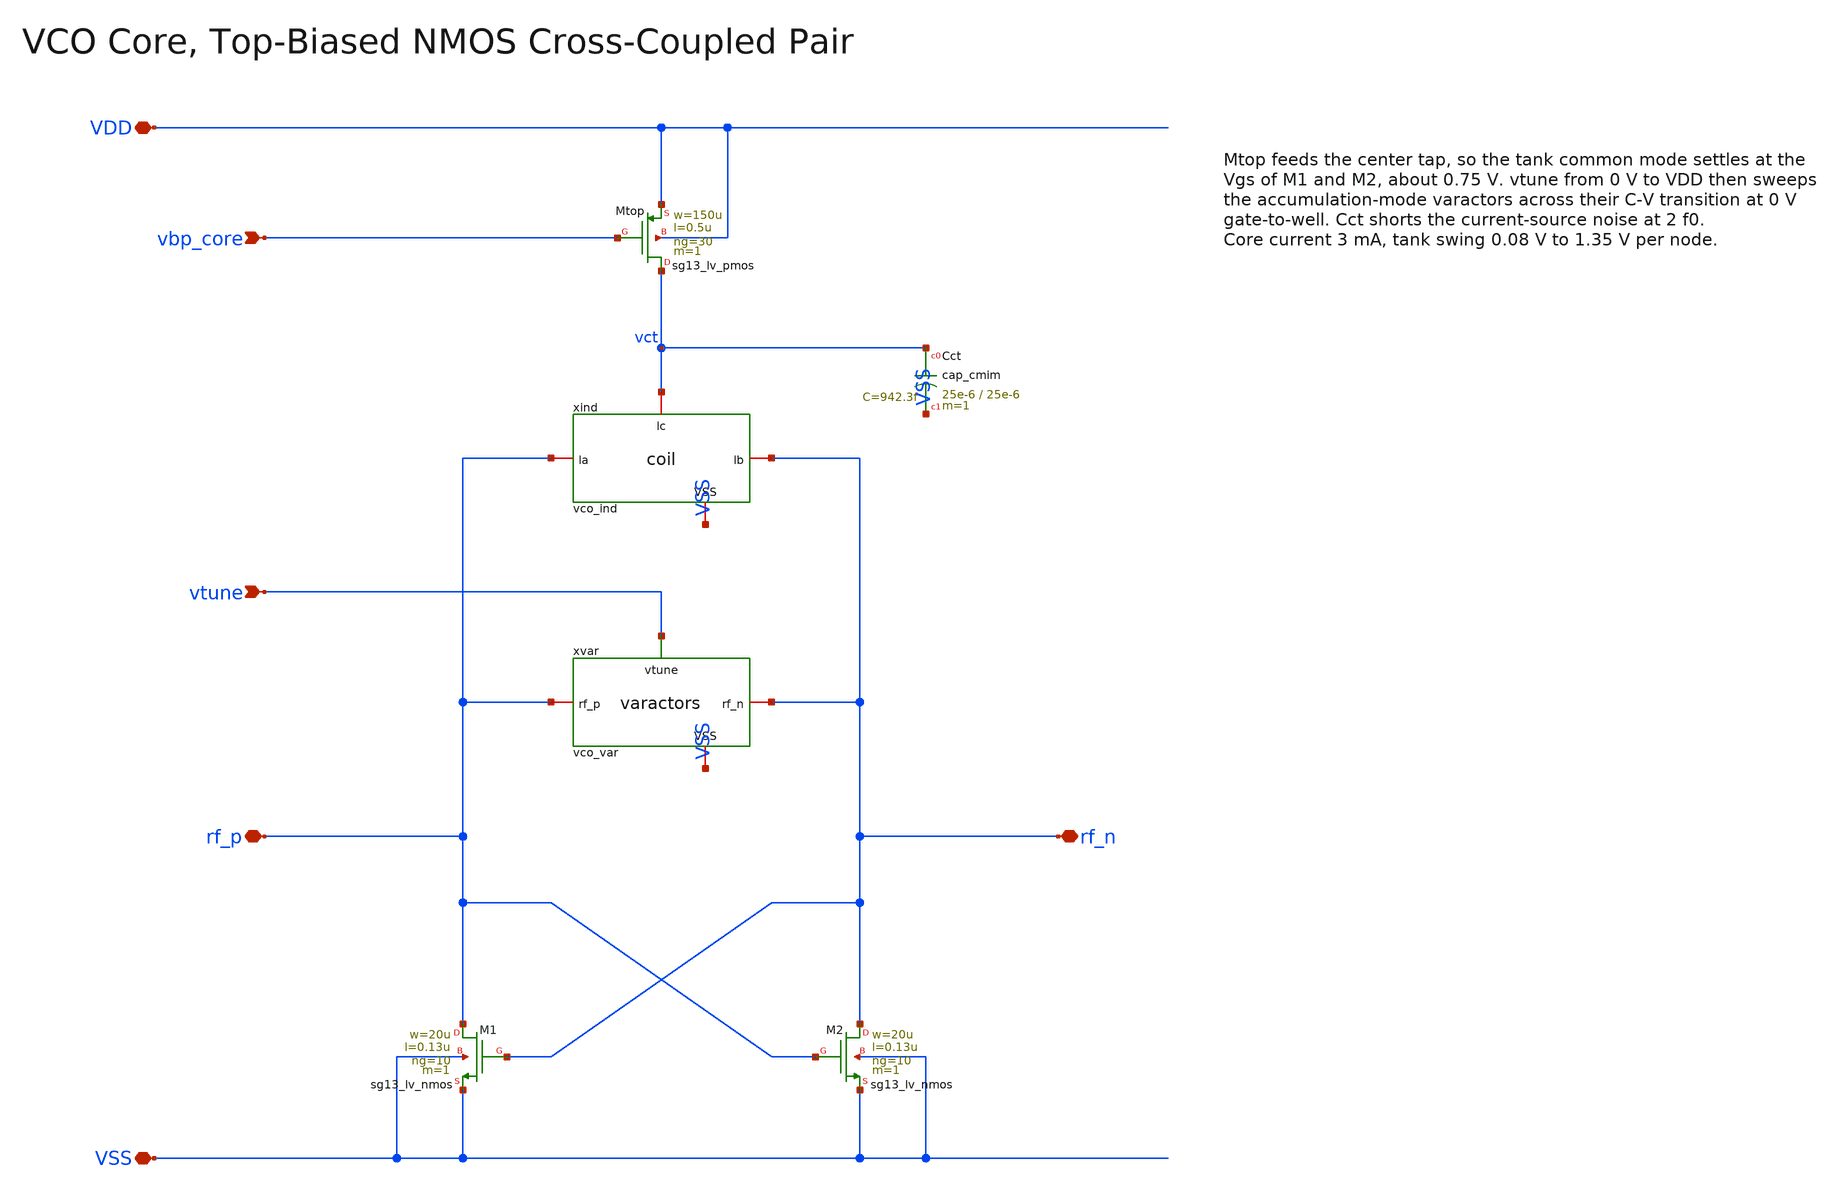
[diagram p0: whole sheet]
** sch_path: macros/vco/schematic/xschem/vco_core.sch
**.subckt vco_core VDD VSS vbp_core vtune rf_p rf_n
*.iopin VDD
*.iopin VSS
*.ipin vbp_core
*.ipin vtune
*.iopin rf_p
*.iopin rf_n
XMtop vct vbp_core VDD VDD sg13_lv_pmos w=150u l=0.5u ng=30 m=1 mm_ok=1
xind rf_p rf_n vct VSS vco_ind
XCct vct VSS cap_cmim w=25e-6 l=25e-6 m=1 mm_ok=1
xvar rf_p rf_n vtune VSS vco_var
XM1 rf_p rf_n VSS VSS sg13_lv_nmos w=20u l=0.13u ng=10 m=1 mm_ok=1
XM2 rf_n rf_p VSS VSS sg13_lv_nmos w=20u l=0.13u ng=10 m=1 mm_ok=1
**.ends

* expanding   symbol:  vco_ind.sym # of pins=4
** sym_path: macros/vco/schematic/xschem/vco_ind.sym
** sch_path: macros/vco/schematic/xschem/vco_ind.sch
.subckt vco_ind la lb lc VSS
*.iopin la
*.iopin lc
*.iopin lb
*.iopin VSS
XL1 la lc lb VSS inductor3 w=4e-6 s=4e-6 d=82e-6 nr_r=2 m=1
x1 la lb lc vco_ind_le
.ends


* expanding   symbol:  vco_var.sym # of pins=4
** sym_path: macros/vco/schematic/xschem/vco_var.sym
** sch_path: macros/vco/schematic/xschem/vco_var.sch
.subckt vco_var rf_p rf_n vtune VSS
*.ipin vtune
*.iopin rf_p
*.iopin rf_n
*.iopin VSS
XCvar1 rf_p vtune rf_n VSS sg13_hv_svaricap w=3.74u l=0.3u Nx=8 mm_ok=1
XCvar2 rf_p vtune rf_n VSS sg13_hv_svaricap w=3.74u l=0.3u Nx=8 mm_ok=1
XCvar3 rf_p vtune rf_n VSS sg13_hv_svaricap w=3.74u l=0.3u Nx=8 mm_ok=1
.ends

.end
